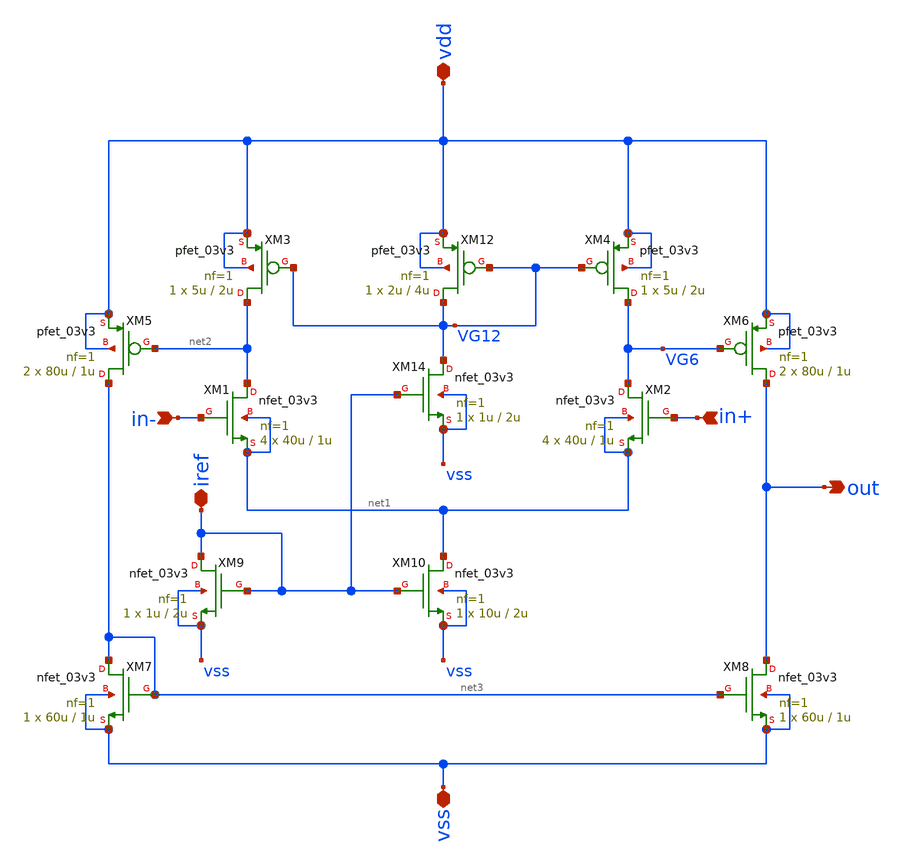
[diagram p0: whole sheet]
** sch_path: Marcel/designs/Two_Stage_OP.sch
**.subckt Two_Stage_OP out in- in+ vdd vss iref
*.opin out
*.ipin in-
*.ipin in+
*.iopin vdd
*.iopin vss
*.iopin iref
XM1 net2 in- net1 net1 nfet_03v3 L=1u W=40u nf=1 ad='int((nf+1)/2) * W/nf * 0.18u' as='int((nf+2)/2) * W/nf * 0.18u'
+ pd='2*int((nf+1)/2) * (W/nf + 0.18u)' ps='2*int((nf+2)/2) * (W/nf + 0.18u)' nrd='0.18u / W' nrs='0.18u / W'
+ sa=0 sb=0 sd=0 m=4
XM2 VG6 in+ net1 net1 nfet_03v3 L=1u W=40u nf=1 ad='int((nf+1)/2) * W/nf * 0.18u' as='int((nf+2)/2) * W/nf * 0.18u'
+ pd='2*int((nf+1)/2) * (W/nf + 0.18u)' ps='2*int((nf+2)/2) * (W/nf + 0.18u)' nrd='0.18u / W' nrs='0.18u / W'
+ sa=0 sb=0 sd=0 m=4
XM3 net2 VG12 vdd vdd pfet_03v3 L=2u W=5u nf=1 ad='int((nf+1)/2) * W/nf * 0.18u' as='int((nf+2)/2) * W/nf * 0.18u'
+ pd='2*int((nf+1)/2) * (W/nf + 0.18u)' ps='2*int((nf+2)/2) * (W/nf + 0.18u)' nrd='0.18u / W' nrs='0.18u / W'
+ sa=0 sb=0 sd=0 m=1
XM4 VG6 VG12 vdd vdd pfet_03v3 L=2u W=5u nf=1 ad='int((nf+1)/2) * W/nf * 0.18u' as='int((nf+2)/2) * W/nf * 0.18u'
+ pd='2*int((nf+1)/2) * (W/nf + 0.18u)' ps='2*int((nf+2)/2) * (W/nf + 0.18u)' nrd='0.18u / W' nrs='0.18u / W'
+ sa=0 sb=0 sd=0 m=1
XM5 net3 net2 vdd vdd pfet_03v3 L=1u W=80u nf=1 ad='int((nf+1)/2) * W/nf * 0.18u' as='int((nf+2)/2) * W/nf * 0.18u'
+ pd='2*int((nf+1)/2) * (W/nf + 0.18u)' ps='2*int((nf+2)/2) * (W/nf + 0.18u)' nrd='0.18u / W' nrs='0.18u / W'
+ sa=0 sb=0 sd=0 m=2
XM6 out VG6 vdd vdd pfet_03v3 L=1u W=80u nf=1 ad='int((nf+1)/2) * W/nf * 0.18u' as='int((nf+2)/2) * W/nf * 0.18u'
+ pd='2*int((nf+1)/2) * (W/nf + 0.18u)' ps='2*int((nf+2)/2) * (W/nf + 0.18u)' nrd='0.18u / W' nrs='0.18u / W'
+ sa=0 sb=0 sd=0 m=2
XM7 net3 net3 vss vss nfet_03v3 L=1u W=60u nf=1 ad='int((nf+1)/2) * W/nf * 0.18u' as='int((nf+2)/2) * W/nf * 0.18u'
+ pd='2*int((nf+1)/2) * (W/nf + 0.18u)' ps='2*int((nf+2)/2) * (W/nf + 0.18u)' nrd='0.18u / W' nrs='0.18u / W'
+ sa=0 sb=0 sd=0 m=1
XM8 out net3 vss vss nfet_03v3 L=1u W=60u nf=1 ad='int((nf+1)/2) * W/nf * 0.18u' as='int((nf+2)/2) * W/nf * 0.18u'
+ pd='2*int((nf+1)/2) * (W/nf + 0.18u)' ps='2*int((nf+2)/2) * (W/nf + 0.18u)' nrd='0.18u / W' nrs='0.18u / W'
+ sa=0 sb=0 sd=0 m=1
XM9 iref iref vss vss nfet_03v3 L=2u W=1u nf=1 ad='int((nf+1)/2) * W/nf * 0.18u' as='int((nf+2)/2) * W/nf * 0.18u'
+ pd='2*int((nf+1)/2) * (W/nf + 0.18u)' ps='2*int((nf+2)/2) * (W/nf + 0.18u)' nrd='0.18u / W' nrs='0.18u / W'
+ sa=0 sb=0 sd=0 m=1
XM10 net1 iref vss vss nfet_03v3 L=2u W=10u nf=1 ad='int((nf+1)/2) * W/nf * 0.18u' as='int((nf+2)/2) * W/nf * 0.18u'
+ pd='2*int((nf+1)/2) * (W/nf + 0.18u)' ps='2*int((nf+2)/2) * (W/nf + 0.18u)' nrd='0.18u / W' nrs='0.18u / W'
+ sa=0 sb=0 sd=0 m=1
XM12 VG12 VG12 vdd vdd pfet_03v3 L=4u W=2u nf=1 ad='int((nf+1)/2) * W/nf * 0.18u' as='int((nf+2)/2) * W/nf * 0.18u'
+ pd='2*int((nf+1)/2) * (W/nf + 0.18u)' ps='2*int((nf+2)/2) * (W/nf + 0.18u)' nrd='0.18u / W' nrs='0.18u / W'
+ sa=0 sb=0 sd=0 m=1
XM14 VG12 iref vss vss nfet_03v3 L=2u W=1u nf=1 ad='int((nf+1)/2) * W/nf * 0.18u' as='int((nf+2)/2) * W/nf * 0.18u'
+ pd='2*int((nf+1)/2) * (W/nf + 0.18u)' ps='2*int((nf+2)/2) * (W/nf + 0.18u)' nrd='0.18u / W' nrs='0.18u / W'
+ sa=0 sb=0 sd=0 m=1
**.ends
.end
